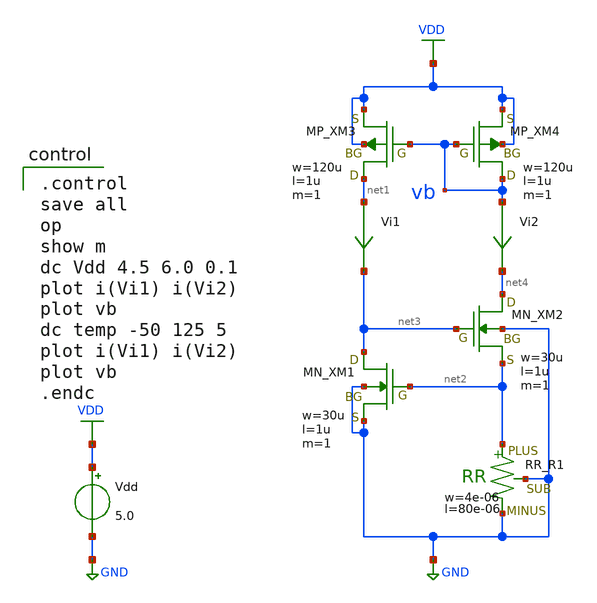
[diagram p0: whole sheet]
** sch_path: TR10/current-source/cs-vth-ref.sch
**.subckt cs-vth-ref
Vdd VDD GND 5.0
Vi1 net1 net3 0
.save i(vi1)
Vi2 vb net4 0
.save i(vi2)
XM1 net3 net2 GND GND NMOS w=30u l=1u as=0 ad=0 ps=0 pd=0 nrd=0 nrs=0 m=1
XM2 net4 net3 net2 GND NMOS w=30u l=1u as=0 ad=0 ps=0 pd=0 nrd=0 nrs=0 m=1
XM3 net1 vb VDD VDD PMOS w=120u l=1u as=0 ad=0 ps=0 pd=0 nrd=0 nrs=0 m=1
XM4 vb vb VDD VDD PMOS w=120u l=1u as=0 ad=0 ps=0 pd=0 nrd=0 nrs=0 m=1
XR1 net2 GND GND F_RR w=4e-06 R=1 l=80e-06 tc1=0 tc2=0
**** begin user architecture code

.control
save all
op
show m
dc Vdd 4.5 6.0 0.1
plot i(Vi1) i(Vi2)
plot vb
dc temp -50 125 5
plot i(Vi1) i(Vi2)
plot vb
.endc

 .include $::LIB/../ip62_models
**** end user architecture code
**.ends
.GLOBAL GND
.GLOBAL VDD
.end
